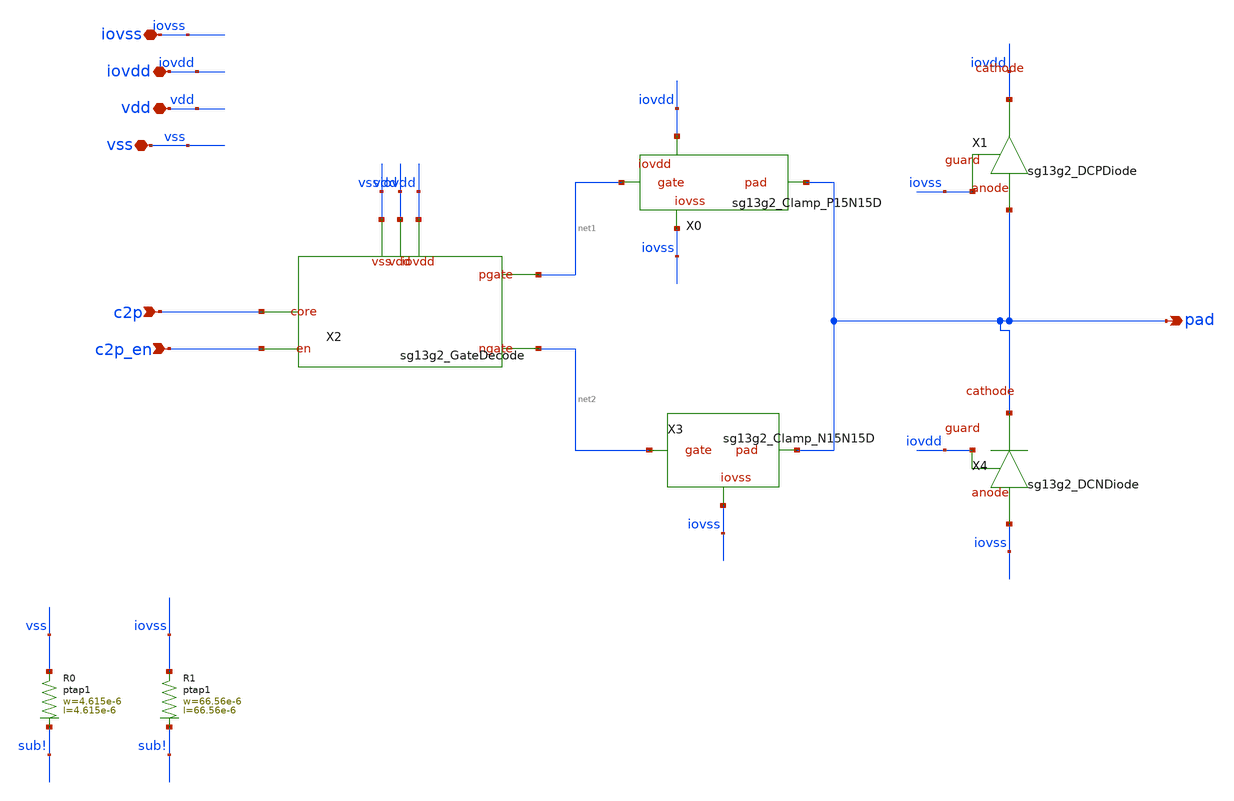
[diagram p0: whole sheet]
** sch_path: ihp-sg13g2/libs.ref/sg13g2_io/sch/xschem/sg13g2_IOPadTriOut30mA.sch
**.subckt sg13g2_IOPadTriOut30mA vdd vss iovdd c2p pad iovss c2p_en
*.iopin vdd
*.iopin vss
*.iopin iovdd
*.ipin c2p
*.opin pad
*.iopin iovss
*.ipin c2p_en
X0 pad net1 iovss iovdd sg13g2_Clamp_P15N15D
X1 iovss iovdd pad sg13g2_DCPDiode
X2 c2p_en c2p net1 net2 vss vdd iovdd sg13g2_GateDecode
X3 pad net2 iovss sg13g2_Clamp_N15N15D
X4 iovdd pad iovss sg13g2_DCNDiode
XR0 vss sub! ptap1 R=24.65 w=4.615e-6 l=4.615e-6
XR1 iovss sub! ptap1 R=208.7m w=66.56e-6 l=66.56e-6
**.ends
.end
